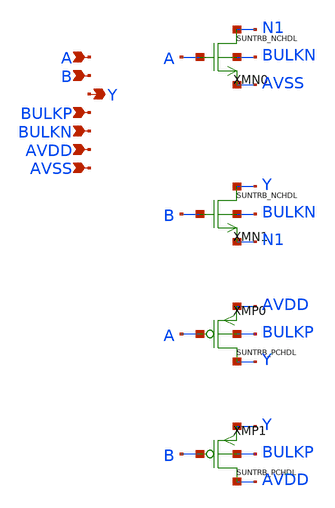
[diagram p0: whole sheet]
** sch_path: design/SUN_TRB_SKY130NM/SUNTRB_NDX1_CV.sch
**.subckt SUNTRB_NDX1_CV A B Y BULKP BULKN AVDD AVSS
*.ipin A
*.ipin B
*.opin Y
*.ipin BULKP
*.ipin BULKN
*.ipin AVDD
*.ipin AVSS
XMN0 N1 A AVSS BULKN SUNTRB_NCHDL xoffset=0 yoffset=0 angle=0
XMN1 Y B N1 BULKN SUNTRB_NCHDL xoffset=0 yoffset=0 angle=0
XMP0 Y A AVDD BULKP SUNTRB_PCHDL xoffset=0 yoffset=0 angle=0 M=1
XMP1 AVDD B Y BULKP SUNTRB_PCHDL xoffset=0 yoffset=0 angle=0 M=1
**.ends
.end
